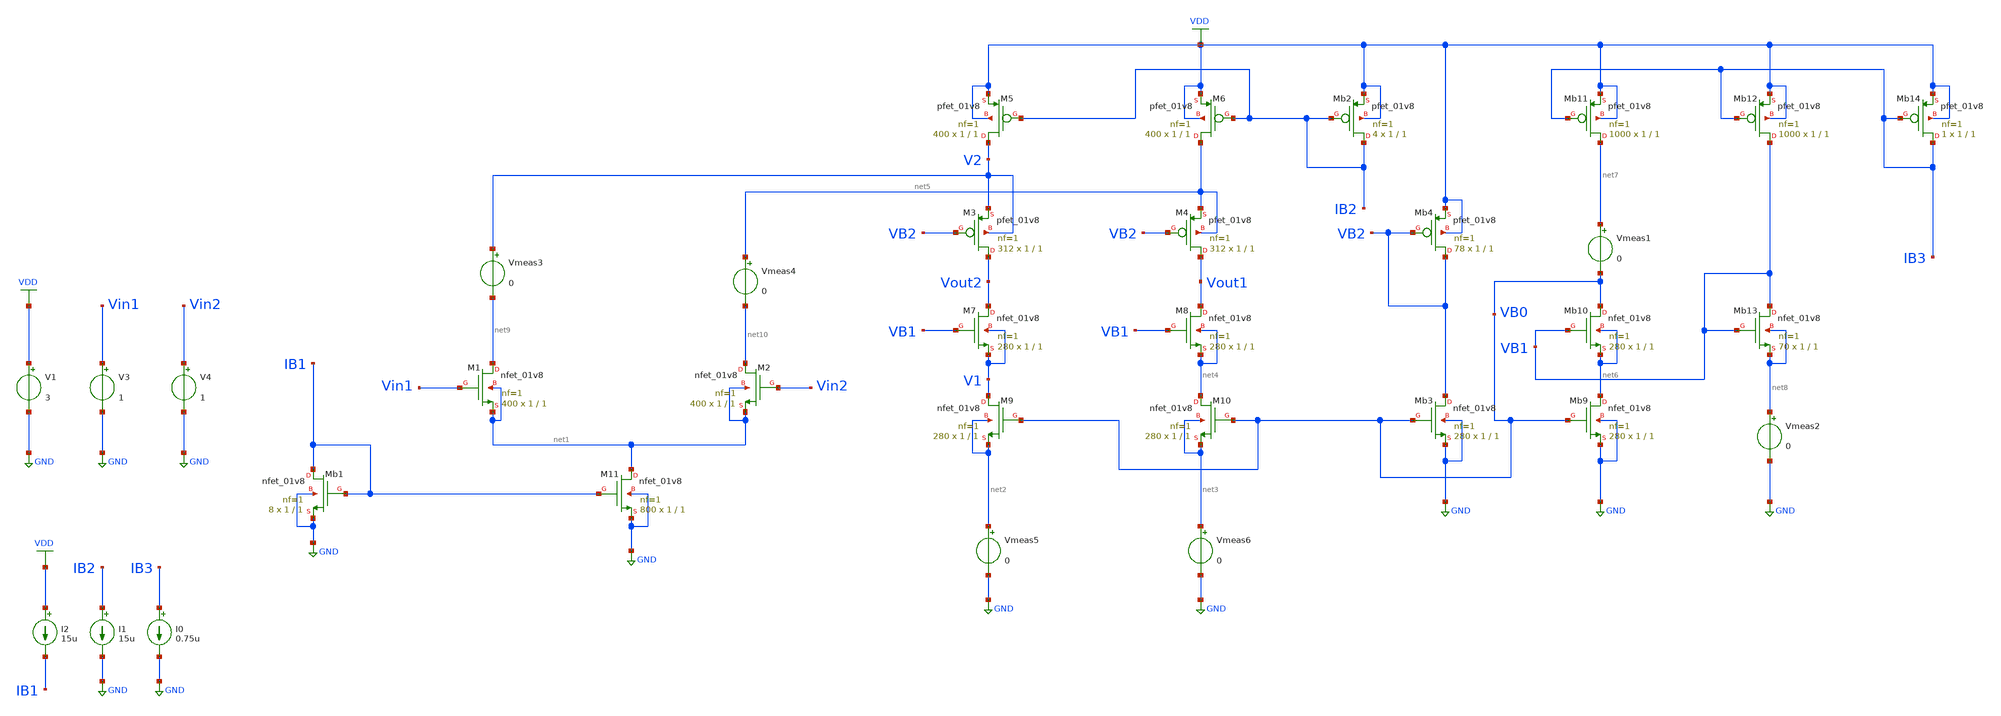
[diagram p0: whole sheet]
** sch_path: Circuits/Examples/Analog/Folded_Cascode/Folded_Cascode.sch
**.subckt Folded_Cascode
V1 VDD GND 3
XM11 net1 IB1 GND GND sky130_fd_pr__nfet_01v8 L=1 W=1 nf=1 ad='int((nf+1)/2) * W/nf * 0.29' as='int((nf+2)/2) * W/nf * 0.29'
+ pd='2*int((nf+1)/2) * (W/nf + 0.29)' ps='2*int((nf+2)/2) * (W/nf + 0.29)' nrd='0.29 / W' nrs='0.29 / W'
+ sa=0 sb=0 sd=0 mult=800 m=800
XM1 net9 Vin1 net1 net1 sky130_fd_pr__nfet_01v8 L=1 W=1 nf=1 ad='int((nf+1)/2) * W/nf * 0.29' as='int((nf+2)/2) * W/nf * 0.29'
+ pd='2*int((nf+1)/2) * (W/nf + 0.29)' ps='2*int((nf+2)/2) * (W/nf + 0.29)' nrd='0.29 / W' nrs='0.29 / W'
+ sa=0 sb=0 sd=0 mult=400 m=400
XM2 net10 Vin2 net1 net1 sky130_fd_pr__nfet_01v8 L=1 W=1 nf=1 ad='int((nf+1)/2) * W/nf * 0.29' as='int((nf+2)/2) * W/nf * 0.29'
+ pd='2*int((nf+1)/2) * (W/nf + 0.29)' ps='2*int((nf+2)/2) * (W/nf + 0.29)' nrd='0.29 / W' nrs='0.29 / W'
+ sa=0 sb=0 sd=0 mult=400 m=400
XM9 V1 VB0 net2 net2 sky130_fd_pr__nfet_01v8 L=1 W=1 nf=1 ad='int((nf+1)/2) * W/nf * 0.29' as='int((nf+2)/2) * W/nf * 0.29'
+ pd='2*int((nf+1)/2) * (W/nf + 0.29)' ps='2*int((nf+2)/2) * (W/nf + 0.29)' nrd='0.29 / W' nrs='0.29 / W'
+ sa=0 sb=0 sd=0 mult=280 m=280
XM10 net4 VB0 net3 net3 sky130_fd_pr__nfet_01v8 L=1 W=1 nf=1 ad='int((nf+1)/2) * W/nf * 0.29' as='int((nf+2)/2) * W/nf * 0.29'
+ pd='2*int((nf+1)/2) * (W/nf + 0.29)' ps='2*int((nf+2)/2) * (W/nf + 0.29)' nrd='0.29 / W' nrs='0.29 / W'
+ sa=0 sb=0 sd=0 mult=280 m=280
XM7 Vout2 VB1 V1 V1 sky130_fd_pr__nfet_01v8 L=1 W=1 nf=1 ad='int((nf+1)/2) * W/nf * 0.29' as='int((nf+2)/2) * W/nf * 0.29'
+ pd='2*int((nf+1)/2) * (W/nf + 0.29)' ps='2*int((nf+2)/2) * (W/nf + 0.29)' nrd='0.29 / W' nrs='0.29 / W'
+ sa=0 sb=0 sd=0 mult=280 m=280
XM8 Vout1 VB1 net4 net4 sky130_fd_pr__nfet_01v8 L=1 W=1 nf=1 ad='int((nf+1)/2) * W/nf * 0.29' as='int((nf+2)/2) * W/nf * 0.29'
+ pd='2*int((nf+1)/2) * (W/nf + 0.29)' ps='2*int((nf+2)/2) * (W/nf + 0.29)' nrd='0.29 / W' nrs='0.29 / W'
+ sa=0 sb=0 sd=0 mult=280 m=280
XM3 Vout2 VB2 V2 V2 sky130_fd_pr__pfet_01v8 L=1 W=1 nf=1 ad='int((nf+1)/2) * W/nf * 0.29' as='int((nf+2)/2) * W/nf * 0.29'
+ pd='2*int((nf+1)/2) * (W/nf + 0.29)' ps='2*int((nf+2)/2) * (W/nf + 0.29)' nrd='0.29 / W' nrs='0.29 / W'
+ sa=0 sb=0 sd=0 mult=312 m=312
XM4 Vout1 VB2 net5 net5 sky130_fd_pr__pfet_01v8 L=1 W=1 nf=1 ad='int((nf+1)/2) * W/nf * 0.29' as='int((nf+2)/2) * W/nf * 0.29'
+ pd='2*int((nf+1)/2) * (W/nf + 0.29)' ps='2*int((nf+2)/2) * (W/nf + 0.29)' nrd='0.29 / W' nrs='0.29 / W'
+ sa=0 sb=0 sd=0 mult=312 m=312
XM5 V2 IB2 VDD VDD sky130_fd_pr__pfet_01v8 L=1 W=1 nf=1 ad='int((nf+1)/2) * W/nf * 0.29' as='int((nf+2)/2) * W/nf * 0.29'
+ pd='2*int((nf+1)/2) * (W/nf + 0.29)' ps='2*int((nf+2)/2) * (W/nf + 0.29)' nrd='0.29 / W' nrs='0.29 / W'
+ sa=0 sb=0 sd=0 mult=400 m=400
XM6 net5 IB2 VDD VDD sky130_fd_pr__pfet_01v8 L=1 W=1 nf=1 ad='int((nf+1)/2) * W/nf * 0.29' as='int((nf+2)/2) * W/nf * 0.29'
+ pd='2*int((nf+1)/2) * (W/nf + 0.29)' ps='2*int((nf+2)/2) * (W/nf + 0.29)' nrd='0.29 / W' nrs='0.29 / W'
+ sa=0 sb=0 sd=0 mult=400 m=400
XMb2 IB2 IB2 VDD VDD sky130_fd_pr__pfet_01v8 L=1 W=1 nf=1 ad='int((nf+1)/2) * W/nf * 0.29' as='int((nf+2)/2) * W/nf * 0.29'
+ pd='2*int((nf+1)/2) * (W/nf + 0.29)' ps='2*int((nf+2)/2) * (W/nf + 0.29)' nrd='0.29 / W' nrs='0.29 / W'
+ sa=0 sb=0 sd=0 mult=4 m=4
XMb1 IB1 IB1 GND GND sky130_fd_pr__nfet_01v8 L=1 W=1 nf=1 ad='int((nf+1)/2) * W/nf * 0.29' as='int((nf+2)/2) * W/nf * 0.29'
+ pd='2*int((nf+1)/2) * (W/nf + 0.29)' ps='2*int((nf+2)/2) * (W/nf + 0.29)' nrd='0.29 / W' nrs='0.29 / W'
+ sa=0 sb=0 sd=0 mult=8 m=8
I0 IB3 GND 0.75u
I1 IB2 GND 15u
I2 VDD IB1 15u
V3 Vin1 GND 1
V4 Vin2 GND 1
XMb9 net6 VB0 GND GND sky130_fd_pr__nfet_01v8 L=1 W=1 nf=1 ad='int((nf+1)/2) * W/nf * 0.29' as='int((nf+2)/2) * W/nf * 0.29'
+ pd='2*int((nf+1)/2) * (W/nf + 0.29)' ps='2*int((nf+2)/2) * (W/nf + 0.29)' nrd='0.29 / W' nrs='0.29 / W'
+ sa=0 sb=0 sd=0 mult=280 m=280
XMb10 VB0 VB1 net6 net6 sky130_fd_pr__nfet_01v8 L=1 W=1 nf=1 ad='int((nf+1)/2) * W/nf * 0.29' as='int((nf+2)/2) * W/nf * 0.29'
+ pd='2*int((nf+1)/2) * (W/nf + 0.29)' ps='2*int((nf+2)/2) * (W/nf + 0.29)' nrd='0.29 / W' nrs='0.29 / W'
+ sa=0 sb=0 sd=0 mult=280 m=280
XMb11 net7 IB3 VDD VDD sky130_fd_pr__pfet_01v8 L=1 W=1 nf=1 ad='int((nf+1)/2) * W/nf * 0.29' as='int((nf+2)/2) * W/nf * 0.29'
+ pd='2*int((nf+1)/2) * (W/nf + 0.29)' ps='2*int((nf+2)/2) * (W/nf + 0.29)' nrd='0.29 / W' nrs='0.29 / W'
+ sa=0 sb=0 sd=0 mult=1000 m=1000
XMb12 VB1 IB3 VDD VDD sky130_fd_pr__pfet_01v8 L=1 W=1 nf=1 ad='int((nf+1)/2) * W/nf * 0.29' as='int((nf+2)/2) * W/nf * 0.29'
+ pd='2*int((nf+1)/2) * (W/nf + 0.29)' ps='2*int((nf+2)/2) * (W/nf + 0.29)' nrd='0.29 / W' nrs='0.29 / W'
+ sa=0 sb=0 sd=0 mult=1000 m=1000
XMb13 VB1 VB1 net8 net8 sky130_fd_pr__nfet_01v8 L=1 W=1 nf=1 ad='int((nf+1)/2) * W/nf * 0.29' as='int((nf+2)/2) * W/nf * 0.29'
+ pd='2*int((nf+1)/2) * (W/nf + 0.29)' ps='2*int((nf+2)/2) * (W/nf + 0.29)' nrd='0.29 / W' nrs='0.29 / W'
+ sa=0 sb=0 sd=0 mult=70 m=70
XMb14 IB3 IB3 VDD VDD sky130_fd_pr__pfet_01v8 L=1 W=1 nf=1 ad='int((nf+1)/2) * W/nf * 0.29' as='int((nf+2)/2) * W/nf * 0.29'
+ pd='2*int((nf+1)/2) * (W/nf + 0.29)' ps='2*int((nf+2)/2) * (W/nf + 0.29)' nrd='0.29 / W' nrs='0.29 / W'
+ sa=0 sb=0 sd=0 mult=1 m=1
Vmeas1 net7 VB0 0
Vmeas2 net8 GND 0
XMb3 VB2 VB0 GND GND sky130_fd_pr__nfet_01v8 L=1 W=1 nf=1 ad='int((nf+1)/2) * W/nf * 0.29' as='int((nf+2)/2) * W/nf * 0.29'
+ pd='2*int((nf+1)/2) * (W/nf + 0.29)' ps='2*int((nf+2)/2) * (W/nf + 0.29)' nrd='0.29 / W' nrs='0.29 / W'
+ sa=0 sb=0 sd=0 mult=280 m=280
XMb4 VB2 VB2 VDD VDD sky130_fd_pr__pfet_01v8 L=1 W=1 nf=1 ad='int((nf+1)/2) * W/nf * 0.29' as='int((nf+2)/2) * W/nf * 0.29'
+ pd='2*int((nf+1)/2) * (W/nf + 0.29)' ps='2*int((nf+2)/2) * (W/nf + 0.29)' nrd='0.29 / W' nrs='0.29 / W'
+ sa=0 sb=0 sd=0 mult=78 m=78
Vmeas3 V2 net9 0
Vmeas4 net5 net10 0
Vmeas5 net2 GND 0
Vmeas6 net3 GND 0
**** begin user architecture code
 ** manual skywater pdks install (with patches applied)
* .lib $::SKYWATER_MODELS/models/sky130.lib.spice tt

** opencircuitdesign pdks install
.lib $::SKYWATER_MODELS/sky130.lib.spice tt

.param mc_mm_switch=0
.param mc_pr_switch=0


.tran 10u 1
.control
run
plot v(V1)
plot (v(Vout2)-v(V1))
plot (v(V2)-v(Vout2))
.endc
.save all

**** end user architecture code
**.ends
.GLOBAL GND
.GLOBAL VDD
.end
